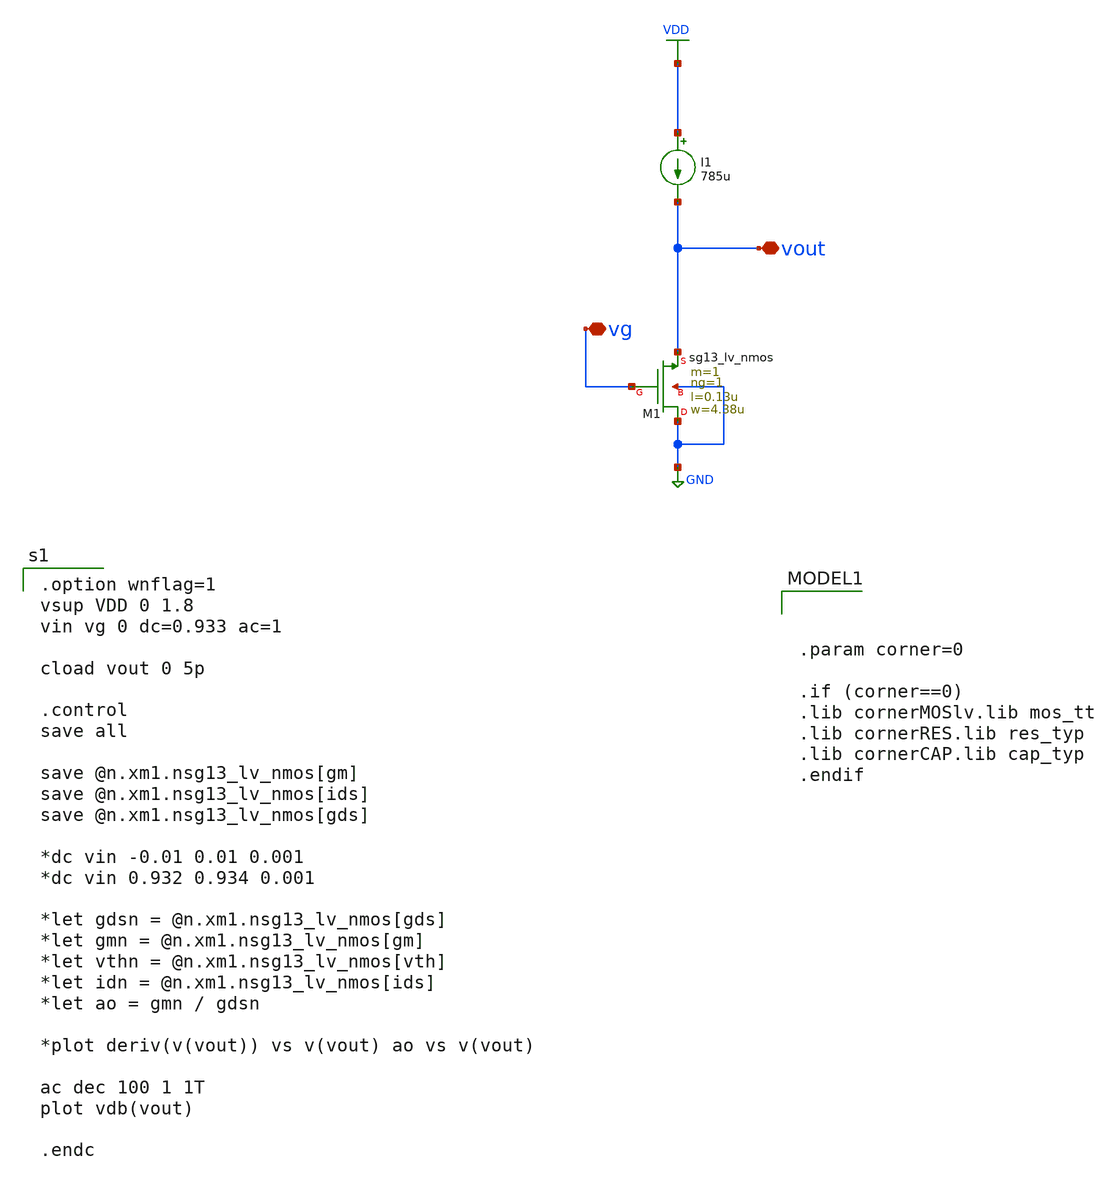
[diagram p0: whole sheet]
** sch_path: xschem/Tareas/Tarea_1/cs_amp_full_IPD413HW1_v2.sch
**.subckt cs_amp_full_IPD413HW1_v2 vg vout
*.iopin vg
*.iopin vout
I1 VDD vout 785u
XM1 GND vg vout GND sg13_lv_nmos w=4.38u l=0.13u ng=1 m=1 mm_ok=1
**** begin user architecture code

.option wnflag=1
vsup VDD 0 1.8
vin vg 0 dc=0.933 ac=1

cload vout 0 5p

.control
save all

save @n.xm1.nsg13_lv_nmos[gm]
save @n.xm1.nsg13_lv_nmos[ids]
save @n.xm1.nsg13_lv_nmos[gds]

*dc vin -0.01 0.01 0.001
*dc vin 0.932 0.934 0.001

*let gdsn = @n.xm1.nsg13_lv_nmos[gds]
*let gmn = @n.xm1.nsg13_lv_nmos[gm]
*let vthn = @n.xm1.nsg13_lv_nmos[vth]
*let idn = @n.xm1.nsg13_lv_nmos[ids]
*let ao = gmn / gdsn

*plot deriv(v(vout)) vs v(vout) ao vs v(vout)

ac dec 100 1 1T
plot vdb(vout)

.endc



.param corner=0

.if (corner==0)
.lib cornerMOSlv.lib mos_tt
.lib cornerRES.lib res_typ
.lib cornerCAP.lib cap_typ
.endif

**** end user architecture code
**.ends
.GLOBAL GND
.GLOBAL VDD
.end
